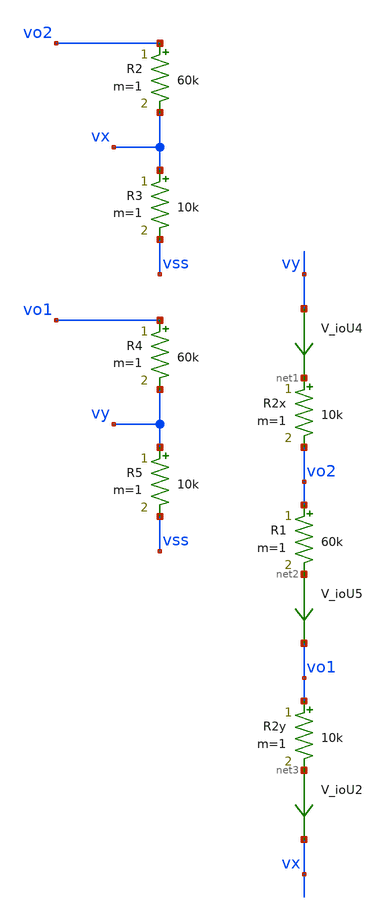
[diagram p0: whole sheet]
** sch_path: xschem/testbenches/bkp.sch
**.subckt bkp
R2x net1 vo2 10k m=1
R1 vo2 net2 60k m=1
R2y vo1 net3 10k m=1
V_ioU2 net3 vx 0
.save i(v_iou2)
V_ioU4 vy net1 0
.save i(v_iou4)
V_ioU5 net2 vo1 0
.save i(v_iou5)
R2 vo2 vx 60k m=1
R3 vx vss 10k m=1
R4 vo1 vy 60k m=1
R5 vy vss 10k m=1
**.ends
.end
